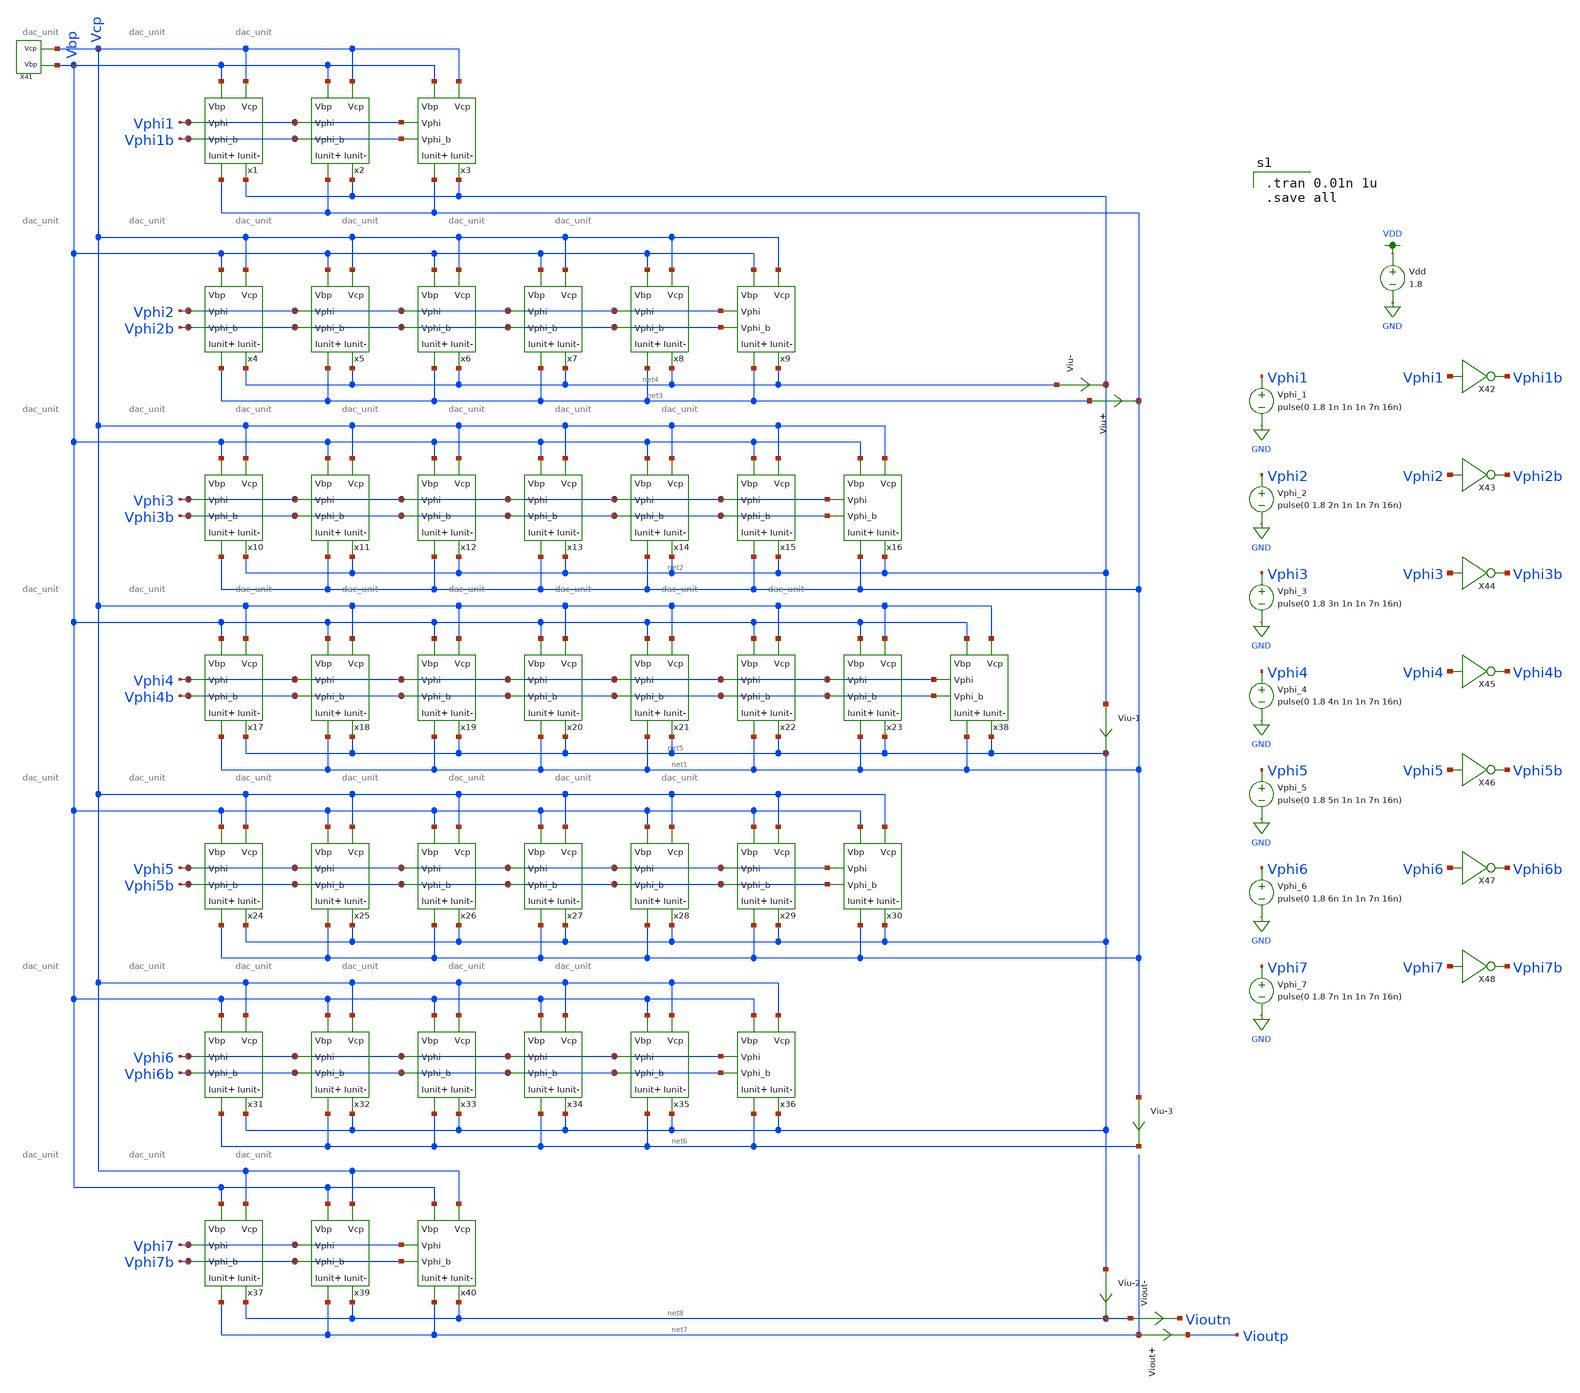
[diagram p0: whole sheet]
** sch_path: simulation/dac/dac.sch
**.subckt dac
x1 Vbp Vcp net1 net2 Vphi1 Vphi1b dac_unit
x2 Vbp Vcp net1 net2 Vphi1 Vphi1b dac_unit
x3 Vbp Vcp net1 net2 Vphi1 Vphi1b dac_unit
x4 Vbp Vcp net3 net4 Vphi2 Vphi2b dac_unit
x5 Vbp Vcp net3 net4 Vphi2 Vphi2b dac_unit
x6 Vbp Vcp net3 net4 Vphi2 Vphi2b dac_unit
x7 Vbp Vcp net3 net4 Vphi2 Vphi2b dac_unit
x8 Vbp Vcp net3 net4 Vphi2 Vphi2b dac_unit
x9 Vbp Vcp net3 net4 Vphi2 Vphi2b dac_unit
x10 Vbp Vcp net1 net2 Vphi3 Vphi3b dac_unit
x11 Vbp Vcp net1 net2 Vphi3 Vphi3b dac_unit
x12 Vbp Vcp net1 net2 Vphi3 Vphi3b dac_unit
x13 Vbp Vcp net1 net2 Vphi3 Vphi3b dac_unit
x14 Vbp Vcp net1 net2 Vphi3 Vphi3b dac_unit
x15 Vbp Vcp net1 net2 Vphi3 Vphi3b dac_unit
x16 Vbp Vcp net1 net2 Vphi3 Vphi3b dac_unit
x17 Vbp Vcp net1 net5 Vphi4 Vphi4b dac_unit
x18 Vbp Vcp net1 net5 Vphi4 Vphi4b dac_unit
x19 Vbp Vcp net1 net5 Vphi4 Vphi4b dac_unit
x20 Vbp Vcp net1 net5 Vphi4 Vphi4b dac_unit
x21 Vbp Vcp net1 net5 Vphi4 Vphi4b dac_unit
x22 Vbp Vcp net1 net5 Vphi4 Vphi4b dac_unit
x23 Vbp Vcp net1 net5 Vphi4 Vphi4b dac_unit
x24 Vbp Vcp net1 net5 Vphi5 Vphi5b dac_unit
x25 Vbp Vcp net1 net5 Vphi5 Vphi5b dac_unit
x26 Vbp Vcp net1 net5 Vphi5 Vphi5b dac_unit
x27 Vbp Vcp net1 net5 Vphi5 Vphi5b dac_unit
x28 Vbp Vcp net1 net5 Vphi5 Vphi5b dac_unit
x29 Vbp Vcp net1 net5 Vphi5 Vphi5b dac_unit
x30 Vbp Vcp net1 net5 Vphi5 Vphi5b dac_unit
x31 Vbp Vcp net6 net5 Vphi6 Vphi6b dac_unit
x32 Vbp Vcp net6 net5 Vphi6 Vphi6b dac_unit
x33 Vbp Vcp net6 net5 Vphi6 Vphi6b dac_unit
x34 Vbp Vcp net6 net5 Vphi6 Vphi6b dac_unit
x35 Vbp Vcp net6 net5 Vphi6 Vphi6b dac_unit
x36 Vbp Vcp net6 net5 Vphi6 Vphi6b dac_unit
x38 Vbp Vcp net1 net5 Vphi4 Vphi4b dac_unit
x37 Vbp Vcp net7 net8 Vphi7 Vphi7b dac_unit
x39 Vbp Vcp net7 net8 Vphi7 Vphi7b dac_unit
x40 Vbp Vcp net7 net8 Vphi7 Vphi7b dac_unit
X41 Vcp Vbp v_gen_lds
Vdd VDD GND 1.8
Vphi_1 Vphi1 GND pulse(0 1.8 1n 1n 1n 7n 16n)
Vphi_2 Vphi2 GND pulse(0 1.8 2n 1n 1n 7n 16n)
Vphi_3 Vphi3 GND pulse(0 1.8 3n 1n 1n 7n 16n)
Vphi_4 Vphi4 GND pulse(0 1.8 4n 1n 1n 7n 16n)
Vphi_5 Vphi5 GND pulse(0 1.8 5n 1n 1n 7n 16n)
Vphi_6 Vphi6 GND pulse(0 1.8 6n 1n 1n 7n 16n)
Vphi_7 Vphi7 GND pulse(0 1.8 7n 1n 1n 7n 16n)
X42 Vphi1 Vphi1b inverter
X43 Vphi2 Vphi2b inverter
X44 Vphi3 Vphi3b inverter
X45 Vphi4 Vphi4b inverter
X46 Vphi5 Vphi5b inverter
X47 Vphi6 Vphi6b inverter
X48 Vphi7 Vphi7b inverter
Viout- net8 Vioutn 0
.save i(viout-)
Viout+ net7 Vioutp 0
.save i(viout+)
Viu- net4 net2 0
.save i(viu-)
Viu+ net3 net1 0
.save i(viu+)
Viu-1 net2 net5 0
.save i(viu-1)
Viu-2 net5 net8 0
.save i(viu-2)
Viu-3 net1 net6 0
.save i(viu-3)
**** begin user architecture code

.tran 0.01n 1u
.save all


.option wnflag=1
.param MC_SWITCH=0.0
.lib ~/skywater/skywater-pdk/libraries/sky130_fd_pr_ngspice/latest/models/sky130.lib.spice tt

**** end user architecture code
**.ends

* expanding   symbol:  ./dac_unit.sym # of pins=6
** sym_path: simulation/dac/dac_unit.sym
** sch_path: simulation/dac/dac_unit.sch
.subckt dac_unit Vbp Vcp Iunit+ Iunit- Vphi Vphi_b
*.ipin Vphi
*.ipin Vbp
*.ipin Vcp
*.opin Iunit-
*.opin Iunit+
*.ipin Vphi_b
XM1 net1 Vbp VDD VDD sky130_fd_pr__pfet_01v8 L=0.5 W=12 nf=1 ad='int((nf+1)/2) * W/nf * 0.29' as='int((nf+2)/2) * W/nf * 0.29'
+ pd='2*int((nf+1)/2) * (W/nf + 0.29)' ps='2*int((nf+2)/2) * (W/nf + 0.29)' nrd='0.29 / W' nrs='0.29 / W'
+ sa=0 sb=0 sd=0 mult=1 m=1
XM2 net2 Vcp net1 VDD sky130_fd_pr__pfet_01v8 L=0.5 W=12 nf=1 ad='int((nf+1)/2) * W/nf * 0.29' as='int((nf+2)/2) * W/nf * 0.29'
+ pd='2*int((nf+1)/2) * (W/nf + 0.29)' ps='2*int((nf+2)/2) * (W/nf + 0.29)' nrd='0.29 / W' nrs='0.29 / W'
+ sa=0 sb=0 sd=0 mult=1 m=1
XM3 Iunit- Vphi net2 VDD sky130_fd_pr__pfet_01v8 L=0.5 W=12 nf=1 ad='int((nf+1)/2) * W/nf * 0.29' as='int((nf+2)/2) * W/nf * 0.29'
+ pd='2*int((nf+1)/2) * (W/nf + 0.29)' ps='2*int((nf+2)/2) * (W/nf + 0.29)' nrd='0.29 / W' nrs='0.29 / W'
+ sa=0 sb=0 sd=0 mult=1 m=1
XM4 Iunit+ Vphi_b net2 VDD sky130_fd_pr__pfet_01v8 L=0.5 W=12 nf=1 ad='int((nf+1)/2) * W/nf * 0.29' as='int((nf+2)/2) * W/nf * 0.29'
+ pd='2*int((nf+1)/2) * (W/nf + 0.29)' ps='2*int((nf+2)/2) * (W/nf + 0.29)' nrd='0.29 / W' nrs='0.29 / W'
+ sa=0 sb=0 sd=0 mult=1 m=1
.ends


* expanding   symbol:  ./v_gen_lds.sym # of pins=2
** sym_path: simulation/dac/v_gen_lds.sym
** sch_path: simulation/dac/v_gen_lds.sch
.subckt v_gen_lds Vcp Vbp
*.opin Vcp
*.opin Vbp
XM25 net1 Vcp Vcp VDD sky130_fd_pr__pfet_01v8 L=0.5 W=12 nf=1 ad='int((nf+1)/2) * W/nf * 0.29' as='int((nf+2)/2) * W/nf * 0.29'
+ pd='2*int((nf+1)/2) * (W/nf + 0.29)' ps='2*int((nf+2)/2) * (W/nf + 0.29)' nrd='0.29 / W' nrs='0.29 / W'
+ sa=0 sb=0 sd=0 mult=1 m=1
XM26 Vcp net3 GND GND sky130_fd_pr__nfet_01v8 L=0.5 W=12 nf=1 ad='int((nf+1)/2) * W/nf * 0.29' as='int((nf+2)/2) * W/nf * 0.29'
+ pd='2*int((nf+1)/2) * (W/nf + 0.29)' ps='2*int((nf+2)/2) * (W/nf + 0.29)' nrd='0.29 / W' nrs='0.29 / W'
+ sa=0 sb=0 sd=0 mult=1 m=1
XM27 net2 net2 net1 VDD sky130_fd_pr__pfet_01v8 L=0.5 W=12 nf=1 ad='int((nf+1)/2) * W/nf * 0.29' as='int((nf+2)/2) * W/nf * 0.29'
+ pd='2*int((nf+1)/2) * (W/nf + 0.29)' ps='2*int((nf+2)/2) * (W/nf + 0.29)' nrd='0.29 / W' nrs='0.29 / W'
+ sa=0 sb=0 sd=0 mult=1 m=1
XM28 GND net3 net4 GND sky130_fd_pr__nfet_01v8 L=0.5 W=12 nf=1 ad='int((nf+1)/2) * W/nf * 0.29' as='int((nf+2)/2) * W/nf * 0.29'
+ pd='2*int((nf+1)/2) * (W/nf + 0.29)' ps='2*int((nf+2)/2) * (W/nf + 0.29)' nrd='0.29 / W' nrs='0.29 / W'
+ sa=0 sb=0 sd=0 mult=1 m=1
XM41 net1 net2 net2 VDD sky130_fd_pr__pfet_01v8 L=0.5 W=12 nf=1 ad='int((nf+1)/2) * W/nf * 0.29' as='int((nf+2)/2) * W/nf * 0.29'
+ pd='2*int((nf+1)/2) * (W/nf + 0.29)' ps='2*int((nf+2)/2) * (W/nf + 0.29)' nrd='0.29 / W' nrs='0.29 / W'
+ sa=0 sb=0 sd=0 mult=1 m=1
XM42 net4 net3 net5 GND sky130_fd_pr__nfet_01v8 L=0.5 W=12 nf=1 ad='int((nf+1)/2) * W/nf * 0.29' as='int((nf+2)/2) * W/nf * 0.29'
+ pd='2*int((nf+1)/2) * (W/nf + 0.29)' ps='2*int((nf+2)/2) * (W/nf + 0.29)' nrd='0.29 / W' nrs='0.29 / W'
+ sa=0 sb=0 sd=0 mult=1 m=1
XM43 net2 net2 net1 VDD sky130_fd_pr__pfet_01v8 L=0.5 W=12 nf=1 ad='int((nf+1)/2) * W/nf * 0.29' as='int((nf+2)/2) * W/nf * 0.29'
+ pd='2*int((nf+1)/2) * (W/nf + 0.29)' ps='2*int((nf+2)/2) * (W/nf + 0.29)' nrd='0.29 / W' nrs='0.29 / W'
+ sa=0 sb=0 sd=0 mult=1 m=1
XM44 net5 net3 net6 GND sky130_fd_pr__nfet_01v8 L=0.5 W=12 nf=1 ad='int((nf+1)/2) * W/nf * 0.29' as='int((nf+2)/2) * W/nf * 0.29'
+ pd='2*int((nf+1)/2) * (W/nf + 0.29)' ps='2*int((nf+2)/2) * (W/nf + 0.29)' nrd='0.29 / W' nrs='0.29 / W'
+ sa=0 sb=0 sd=0 mult=1 m=1
XM45 net1 net2 net2 VDD sky130_fd_pr__pfet_01v8 L=0.5 W=12 nf=1 ad='int((nf+1)/2) * W/nf * 0.29' as='int((nf+2)/2) * W/nf * 0.29'
+ pd='2*int((nf+1)/2) * (W/nf + 0.29)' ps='2*int((nf+2)/2) * (W/nf + 0.29)' nrd='0.29 / W' nrs='0.29 / W'
+ sa=0 sb=0 sd=0 mult=1 m=1
XM46 net6 net3 net7 GND sky130_fd_pr__nfet_01v8 L=0.5 W=12 nf=1 ad='int((nf+1)/2) * W/nf * 0.29' as='int((nf+2)/2) * W/nf * 0.29'
+ pd='2*int((nf+1)/2) * (W/nf + 0.29)' ps='2*int((nf+2)/2) * (W/nf + 0.29)' nrd='0.29 / W' nrs='0.29 / W'
+ sa=0 sb=0 sd=0 mult=1 m=1
XM47 VDD net2 net1 VDD sky130_fd_pr__pfet_01v8 L=0.5 W=12 nf=1 ad='int((nf+1)/2) * W/nf * 0.29' as='int((nf+2)/2) * W/nf * 0.29'
+ pd='2*int((nf+1)/2) * (W/nf + 0.29)' ps='2*int((nf+2)/2) * (W/nf + 0.29)' nrd='0.29 / W' nrs='0.29 / W'
+ sa=0 sb=0 sd=0 mult=1 m=1
XM48 net7 net3 net2 GND sky130_fd_pr__nfet_01v8 L=0.5 W=12 nf=1 ad='int((nf+1)/2) * W/nf * 0.29' as='int((nf+2)/2) * W/nf * 0.29'
+ pd='2*int((nf+1)/2) * (W/nf + 0.29)' ps='2*int((nf+2)/2) * (W/nf + 0.29)' nrd='0.29 / W' nrs='0.29 / W'
+ sa=0 sb=0 sd=0 mult=1 m=1
XM54 VDD Vbp Vbp VDD sky130_fd_pr__pfet_01v8 L=0.5 W=12 nf=1 ad='int((nf+1)/2) * W/nf * 0.29' as='int((nf+2)/2) * W/nf * 0.29'
+ pd='2*int((nf+1)/2) * (W/nf + 0.29)' ps='2*int((nf+2)/2) * (W/nf + 0.29)' nrd='0.29 / W' nrs='0.29 / W'
+ sa=0 sb=0 sd=0 mult=1 m=1
XM1 Vbp net3 GND GND sky130_fd_pr__nfet_01v8 L=0.5 W=12 nf=1 ad='int((nf+1)/2) * W/nf * 0.29' as='int((nf+2)/2) * W/nf * 0.29'
+ pd='2*int((nf+1)/2) * (W/nf + 0.29)' ps='2*int((nf+2)/2) * (W/nf + 0.29)' nrd='0.29 / W' nrs='0.29 / W'
+ sa=0 sb=0 sd=0 mult=1 m=1
XM2 net3 net3 GND GND sky130_fd_pr__nfet_01v8 L=0.5 W=12 nf=1 ad='int((nf+1)/2) * W/nf * 0.29' as='int((nf+2)/2) * W/nf * 0.29'
+ pd='2*int((nf+1)/2) * (W/nf + 0.29)' ps='2*int((nf+2)/2) * (W/nf + 0.29)' nrd='0.29 / W' nrs='0.29 / W'
+ sa=0 sb=0 sd=0 mult=1 m=1
XM3 Vcp VDD VDD VDD sky130_fd_pr__pfet_01v8 L=0.5 W=12 nf=1 ad='int((nf+1)/2) * W/nf * 0.29' as='int((nf+2)/2) * W/nf * 0.29'
+ pd='2*int((nf+1)/2) * (W/nf + 0.29)' ps='2*int((nf+2)/2) * (W/nf + 0.29)' nrd='0.29 / W' nrs='0.29 / W'
+ sa=0 sb=0 sd=0 mult=1 m=1
XM16 net8 net13 net13 VDD sky130_fd_pr__pfet_01v8 L=0.5 W=12 nf=1 ad='int((nf+1)/2) * W/nf * 0.29' as='int((nf+2)/2) * W/nf * 0.29'
+ pd='2*int((nf+1)/2) * (W/nf + 0.29)' ps='2*int((nf+2)/2) * (W/nf + 0.29)' nrd='0.29 / W' nrs='0.29 / W'
+ sa=0 sb=0 sd=0 mult=1 m=1
XM17 net13 net3 GND GND sky130_fd_pr__nfet_01v8 L=0.5 W=12 nf=1 ad='int((nf+1)/2) * W/nf * 0.29' as='int((nf+2)/2) * W/nf * 0.29'
+ pd='2*int((nf+1)/2) * (W/nf + 0.29)' ps='2*int((nf+2)/2) * (W/nf + 0.29)' nrd='0.29 / W' nrs='0.29 / W'
+ sa=0 sb=0 sd=0 mult=1 m=1
XM18 net2 net2 net8 VDD sky130_fd_pr__pfet_01v8 L=0.5 W=12 nf=1 ad='int((nf+1)/2) * W/nf * 0.29' as='int((nf+2)/2) * W/nf * 0.29'
+ pd='2*int((nf+1)/2) * (W/nf + 0.29)' ps='2*int((nf+2)/2) * (W/nf + 0.29)' nrd='0.29 / W' nrs='0.29 / W'
+ sa=0 sb=0 sd=0 mult=1 m=1
XM19 GND net3 net9 GND sky130_fd_pr__nfet_01v8 L=0.5 W=12 nf=1 ad='int((nf+1)/2) * W/nf * 0.29' as='int((nf+2)/2) * W/nf * 0.29'
+ pd='2*int((nf+1)/2) * (W/nf + 0.29)' ps='2*int((nf+2)/2) * (W/nf + 0.29)' nrd='0.29 / W' nrs='0.29 / W'
+ sa=0 sb=0 sd=0 mult=1 m=1
XM20 net8 net2 net2 VDD sky130_fd_pr__pfet_01v8 L=0.5 W=12 nf=1 ad='int((nf+1)/2) * W/nf * 0.29' as='int((nf+2)/2) * W/nf * 0.29'
+ pd='2*int((nf+1)/2) * (W/nf + 0.29)' ps='2*int((nf+2)/2) * (W/nf + 0.29)' nrd='0.29 / W' nrs='0.29 / W'
+ sa=0 sb=0 sd=0 mult=1 m=1
XM21 net9 net3 net10 GND sky130_fd_pr__nfet_01v8 L=0.5 W=12 nf=1 ad='int((nf+1)/2) * W/nf * 0.29' as='int((nf+2)/2) * W/nf * 0.29'
+ pd='2*int((nf+1)/2) * (W/nf + 0.29)' ps='2*int((nf+2)/2) * (W/nf + 0.29)' nrd='0.29 / W' nrs='0.29 / W'
+ sa=0 sb=0 sd=0 mult=1 m=1
XM22 net2 net2 net8 VDD sky130_fd_pr__pfet_01v8 L=0.5 W=12 nf=1 ad='int((nf+1)/2) * W/nf * 0.29' as='int((nf+2)/2) * W/nf * 0.29'
+ pd='2*int((nf+1)/2) * (W/nf + 0.29)' ps='2*int((nf+2)/2) * (W/nf + 0.29)' nrd='0.29 / W' nrs='0.29 / W'
+ sa=0 sb=0 sd=0 mult=1 m=1
XM23 net10 net3 net11 GND sky130_fd_pr__nfet_01v8 L=0.5 W=12 nf=1 ad='int((nf+1)/2) * W/nf * 0.29' as='int((nf+2)/2) * W/nf * 0.29'
+ pd='2*int((nf+1)/2) * (W/nf + 0.29)' ps='2*int((nf+2)/2) * (W/nf + 0.29)' nrd='0.29 / W' nrs='0.29 / W'
+ sa=0 sb=0 sd=0 mult=1 m=1
XM24 net8 net2 net2 VDD sky130_fd_pr__pfet_01v8 L=0.5 W=12 nf=1 ad='int((nf+1)/2) * W/nf * 0.29' as='int((nf+2)/2) * W/nf * 0.29'
+ pd='2*int((nf+1)/2) * (W/nf + 0.29)' ps='2*int((nf+2)/2) * (W/nf + 0.29)' nrd='0.29 / W' nrs='0.29 / W'
+ sa=0 sb=0 sd=0 mult=1 m=1
XM49 net11 net3 net12 GND sky130_fd_pr__nfet_01v8 L=0.5 W=12 nf=1 ad='int((nf+1)/2) * W/nf * 0.29' as='int((nf+2)/2) * W/nf * 0.29'
+ pd='2*int((nf+1)/2) * (W/nf + 0.29)' ps='2*int((nf+2)/2) * (W/nf + 0.29)' nrd='0.29 / W' nrs='0.29 / W'
+ sa=0 sb=0 sd=0 mult=1 m=1
XM50 VDD net2 net8 VDD sky130_fd_pr__pfet_01v8 L=0.5 W=12 nf=1 ad='int((nf+1)/2) * W/nf * 0.29' as='int((nf+2)/2) * W/nf * 0.29'
+ pd='2*int((nf+1)/2) * (W/nf + 0.29)' ps='2*int((nf+2)/2) * (W/nf + 0.29)' nrd='0.29 / W' nrs='0.29 / W'
+ sa=0 sb=0 sd=0 mult=1 m=1
XM51 net12 net3 net2 GND sky130_fd_pr__nfet_01v8 L=0.5 W=12 nf=1 ad='int((nf+1)/2) * W/nf * 0.29' as='int((nf+2)/2) * W/nf * 0.29'
+ pd='2*int((nf+1)/2) * (W/nf + 0.29)' ps='2*int((nf+2)/2) * (W/nf + 0.29)' nrd='0.29 / W' nrs='0.29 / W'
+ sa=0 sb=0 sd=0 mult=1 m=1
XM52 VDD Vbp Vbp VDD sky130_fd_pr__pfet_01v8 L=0.5 W=12 nf=1 ad='int((nf+1)/2) * W/nf * 0.29' as='int((nf+2)/2) * W/nf * 0.29'
+ pd='2*int((nf+1)/2) * (W/nf + 0.29)' ps='2*int((nf+2)/2) * (W/nf + 0.29)' nrd='0.29 / W' nrs='0.29 / W'
+ sa=0 sb=0 sd=0 mult=1 m=1
XM53 GND net3 Vbp GND sky130_fd_pr__nfet_01v8 L=0.5 W=12 nf=1 ad='int((nf+1)/2) * W/nf * 0.29' as='int((nf+2)/2) * W/nf * 0.29'
+ pd='2*int((nf+1)/2) * (W/nf + 0.29)' ps='2*int((nf+2)/2) * (W/nf + 0.29)' nrd='0.29 / W' nrs='0.29 / W'
+ sa=0 sb=0 sd=0 mult=1 m=1
XM55 net3 net3 GND GND sky130_fd_pr__nfet_01v8 L=0.5 W=12 nf=1 ad='int((nf+1)/2) * W/nf * 0.29' as='int((nf+2)/2) * W/nf * 0.29'
+ pd='2*int((nf+1)/2) * (W/nf + 0.29)' ps='2*int((nf+2)/2) * (W/nf + 0.29)' nrd='0.29 / W' nrs='0.29 / W'
+ sa=0 sb=0 sd=0 mult=1 m=1
XM56 net13 VDD VDD VDD sky130_fd_pr__pfet_01v8 L=0.5 W=12 nf=1 ad='int((nf+1)/2) * W/nf * 0.29' as='int((nf+2)/2) * W/nf * 0.29'
+ pd='2*int((nf+1)/2) * (W/nf + 0.29)' ps='2*int((nf+2)/2) * (W/nf + 0.29)' nrd='0.29 / W' nrs='0.29 / W'
+ sa=0 sb=0 sd=0 mult=1 m=1
Ib GND net3 2u
.ends


* expanding   symbol:  ./inverter.sym # of pins=2
** sym_path: simulation/dac/inverter.sym
** sch_path: simulation/dac/inverter.sch
.subckt inverter A Y
*.ipin A
*.opin Y
XM1 Y A VDD VDD sky130_fd_pr__pfet_01v8 L=0.15 W=1 nf=1 ad='int((nf+1)/2) * W/nf * 0.29' as='int((nf+2)/2) * W/nf * 0.29'
+ pd='2*int((nf+1)/2) * (W/nf + 0.29)' ps='2*int((nf+2)/2) * (W/nf + 0.29)' nrd='0.29 / W' nrs='0.29 / W'
+ sa=0 sb=0 sd=0 mult=1 m=1
XM2 Y A GND GND sky130_fd_pr__nfet_01v8 L=0.15 W=1 nf=1 ad='int((nf+1)/2) * W/nf * 0.29' as='int((nf+2)/2) * W/nf * 0.29'
+ pd='2*int((nf+1)/2) * (W/nf + 0.29)' ps='2*int((nf+2)/2) * (W/nf + 0.29)' nrd='0.29 / W' nrs='0.29 / W'
+ sa=0 sb=0 sd=0 mult=1 m=1
.ends

.GLOBAL VDD
.GLOBAL GND
.end
